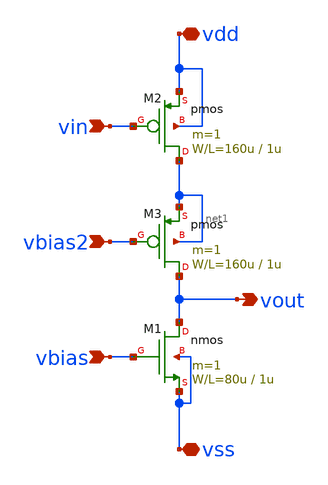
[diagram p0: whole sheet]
** sch_path: member_project/GroupWork/Team_masahiro/pfet_cascode_common_source_load_current.sch
**.subckt pfet_cascode_common_source_load_current vss vdd vin vout vbias vbias2
*.iopin vss
*.iopin vdd
*.ipin vin
*.opin vout
*.ipin vbias
*.ipin vbias2
M1 vout vbias vss vss nmos L=1u W=80u m=1
M2 net1 vin vdd vdd pmos L=1u W=160u m=1
M3 vout vbias2 net1 net1 pmos L=1u W=160u m=1
**** begin user architecture code
 .include $::LIB/mos.lib
.include $::LIB/passive.lib
.include $::LIB/diode.lib
**** end user architecture code
**.ends
.end
